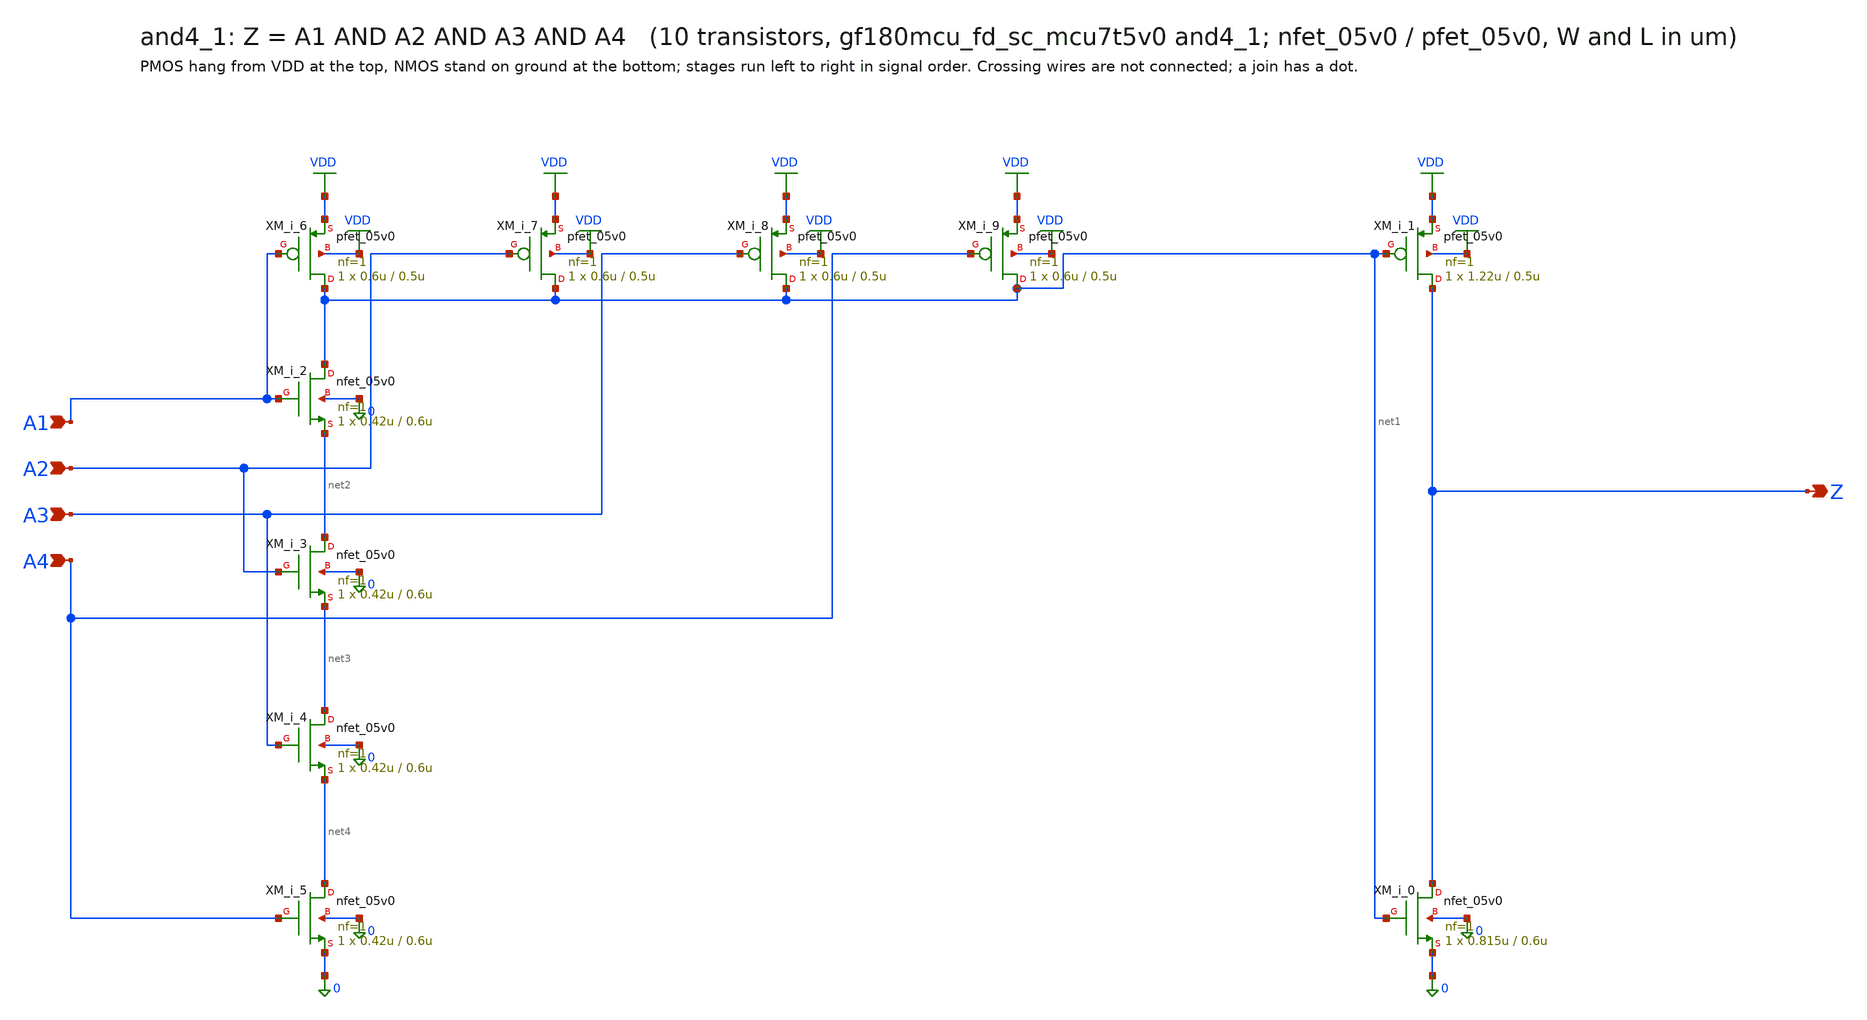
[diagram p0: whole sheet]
** sch_path: xschem/cells_tx/and4_1.sch
**.subckt and4_1 A1 A2 A3 A4 Z
*.ipin A1
*.ipin A2
*.ipin A3
*.ipin A4
*.opin Z
XM_i_2 net1 A1 net2 0 nfet_05v0 L=0.6u W=0.42u nf=1 ad=2.1e-13 as=2.1e-13 pd=1.84e-06 ps=1.84e-06
+ nrd=0 nrs=0 sa=0 sb=0 sd=0 m=1
XM_i_3 net2 A2 net3 0 nfet_05v0 L=0.6u W=0.42u nf=1 ad=2.1e-13 as=2.1e-13 pd=1.84e-06 ps=1.84e-06
+ nrd=0 nrs=0 sa=0 sb=0 sd=0 m=1
XM_i_4 net3 A3 net4 0 nfet_05v0 L=0.6u W=0.42u nf=1 ad=2.1e-13 as=2.1e-13 pd=1.84e-06 ps=1.84e-06
+ nrd=0 nrs=0 sa=0 sb=0 sd=0 m=1
XM_i_5 net4 A4 0 0 nfet_05v0 L=0.6u W=0.42u nf=1 ad=2.1e-13 as=2.1e-13 pd=1.84e-06 ps=1.84e-06 nrd=0
+ nrs=0 sa=0 sb=0 sd=0 m=1
XM_i_0 Z net1 0 0 nfet_05v0 L=0.6u W=0.815u nf=1 ad=4.075e-13 as=4.075e-13 pd=2.63e-06 ps=2.63e-06
+ nrd=0 nrs=0 sa=0 sb=0 sd=0 m=1
XM_i_6 net1 A1 VDD VDD pfet_05v0 L=0.5u W=0.6u nf=1 ad=3e-13 as=3e-13 pd=2.2e-06 ps=2.2e-06 nrd=0
+ nrs=0 sa=0 sb=0 sd=0 m=1
XM_i_7 net1 A2 VDD VDD pfet_05v0 L=0.5u W=0.6u nf=1 ad=3e-13 as=3e-13 pd=2.2e-06 ps=2.2e-06 nrd=0
+ nrs=0 sa=0 sb=0 sd=0 m=1
XM_i_8 net1 A3 VDD VDD pfet_05v0 L=0.5u W=0.6u nf=1 ad=3e-13 as=3e-13 pd=2.2e-06 ps=2.2e-06 nrd=0
+ nrs=0 sa=0 sb=0 sd=0 m=1
XM_i_9 net1 A4 VDD VDD pfet_05v0 L=0.5u W=0.6u nf=1 ad=3e-13 as=3e-13 pd=2.2e-06 ps=2.2e-06 nrd=0
+ nrs=0 sa=0 sb=0 sd=0 m=1
XM_i_1 Z net1 VDD VDD pfet_05v0 L=0.5u W=1.22u nf=1 ad=6.1e-13 as=6.1e-13 pd=3.44e-06 ps=3.44e-06
+ nrd=0 nrs=0 sa=0 sb=0 sd=0 m=1
**.ends
.GLOBAL VDD
.end
